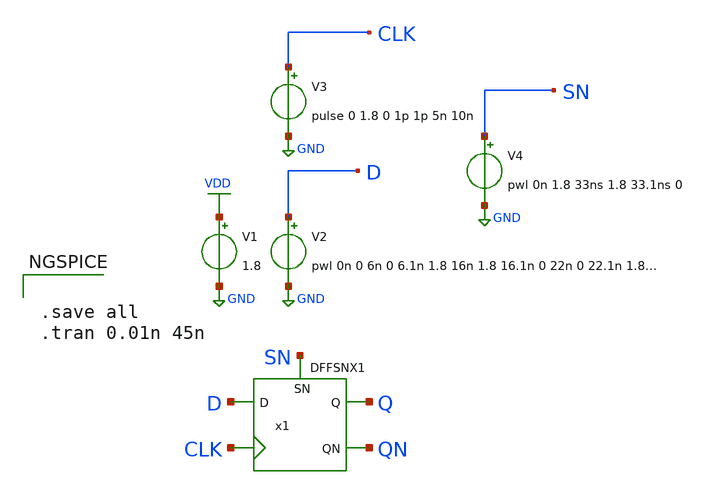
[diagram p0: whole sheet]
** sch_path: layout/xschem/sky130_rhbd/testbenches/test_DFFSNX1.sch
**.subckt test_DFFSNX1
V2 D GND pwl 0n 0 6n 0 6.1n 1.8 16n 1.8 16.1n 0 22n 0 22.1n 1.8 32n 1.8 32.1n 0
V1 VDD GND 1.8
V3 CLK GND pulse 0 1.8 0 1p 1p 5n 10n
V4 SN GND pwl 0n 1.8 33ns 1.8 33.1ns 0
x1 Q QN D CLK SN VDD GND DFFSNX1
**** begin user architecture code

.lib $::SKYWATER_MODELS/sky130.lib.spice tt


**** end user architecture code
**.ends
.GLOBAL VDD
.GLOBAL GND
**** begin user architecture code


.save all
.tran 0.01n 45n


**** end user architecture code
.end
